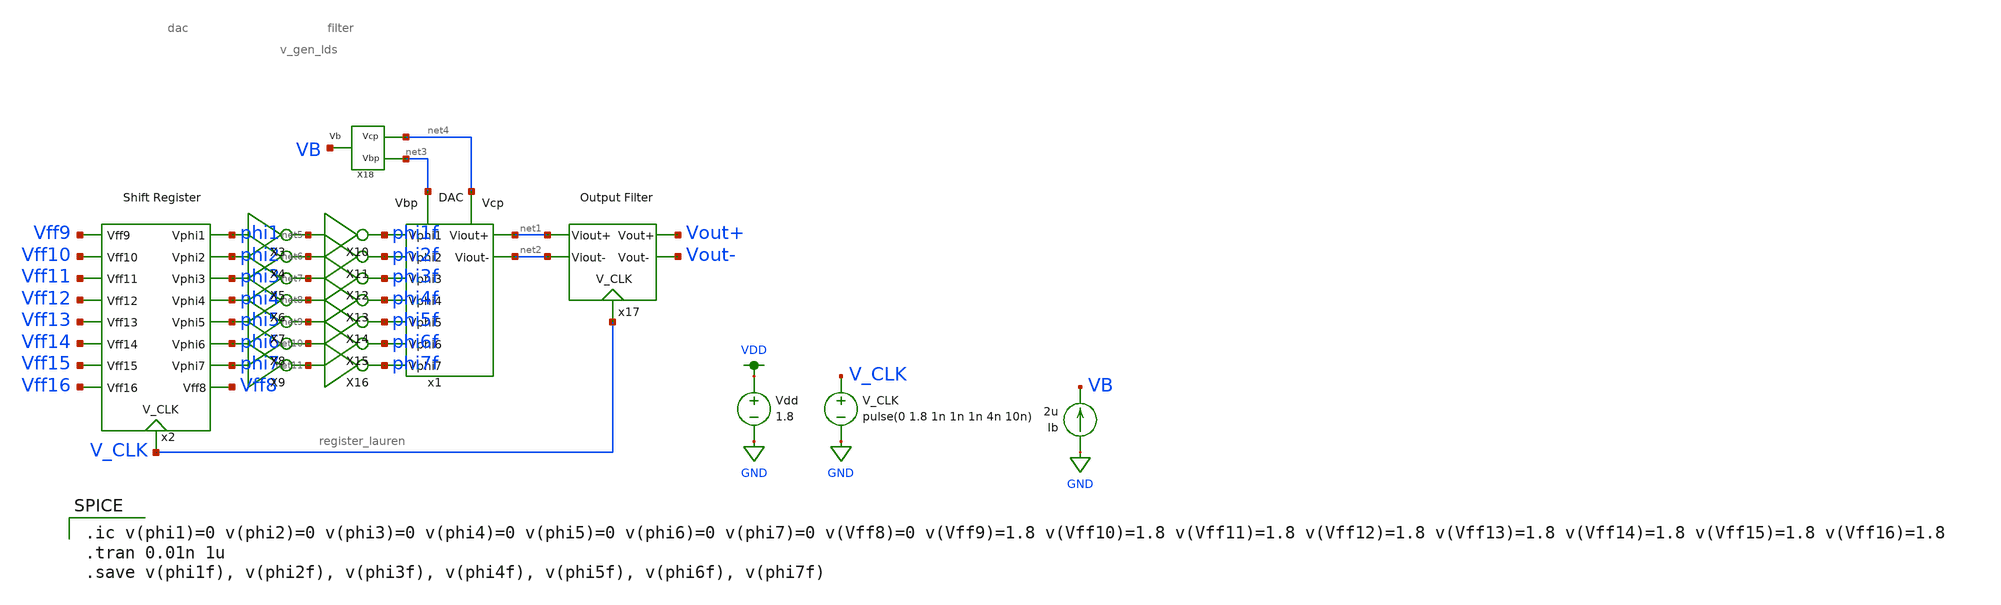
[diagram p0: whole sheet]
** sch_path: simulation/archived/combined_simulations/register_dac_tran_andrew.sch
**.subckt register_dac_tran_andrew
V_CLK V_CLK GND pulse(0 1.8 1n 1n 1n 4n 10n)
Vdd VDD GND 1.8
x1 phi1f phi2f phi3f phi4f phi5f phi6f phi7f net1 net2 net3 net4 dac
x2 Vff10 Vff11 Vff12 Vff13 Vff14 Vff16 Vff15 Vff9 phi1 phi2 phi3 phi4 phi5 phi6 phi7 Vff8 V_CLK
+ register_lauren
X3 phi1 net5 inverter
X4 phi2 net6 inverter
X5 phi3 net7 inverter
X6 phi4 net8 inverter
X7 phi5 net9 inverter
X8 phi6 net10 inverter
X9 phi7 net11 inverter
X10 net5 phi1f inverter
X11 net6 phi2f inverter
X12 net7 phi3f inverter
X13 net8 phi4f inverter
X14 net9 phi5f inverter
X15 net10 phi6f inverter
X16 net11 phi7f inverter
x17 net1 net2 Vout+ Vout- V_CLK filter
X18 net4 net3 VB v_gen_lds
Ib GND VB 2u
**** begin user architecture code

.option wnflag=1
.param MC_SWITCH=0.0
.lib ~/skywater/skywater-pdk/libraries/sky130_fd_pr_ngspice/latest/models/sky130.lib.spice tt


.ic v(phi1)=0 v(phi2)=0 v(phi3)=0 v(phi4)=0 v(phi5)=0 v(phi6)=0 v(phi7)=0 v(Vff8)=0 v(Vff9)=1.8
+ v(Vff10)=1.8 v(Vff11)=1.8 v(Vff12)=1.8 v(Vff13)=1.8 v(Vff14)=1.8 v(Vff15)=1.8 v(Vff16)=1.8
.tran 0.01n 1u
.save v(phi1f), v(phi2f), v(phi3f), v(phi4f), v(phi5f), v(phi6f), v(phi7f)

**** end user architecture code
**.ends
.GLOBAL GND
.GLOBAL VDD
.end
